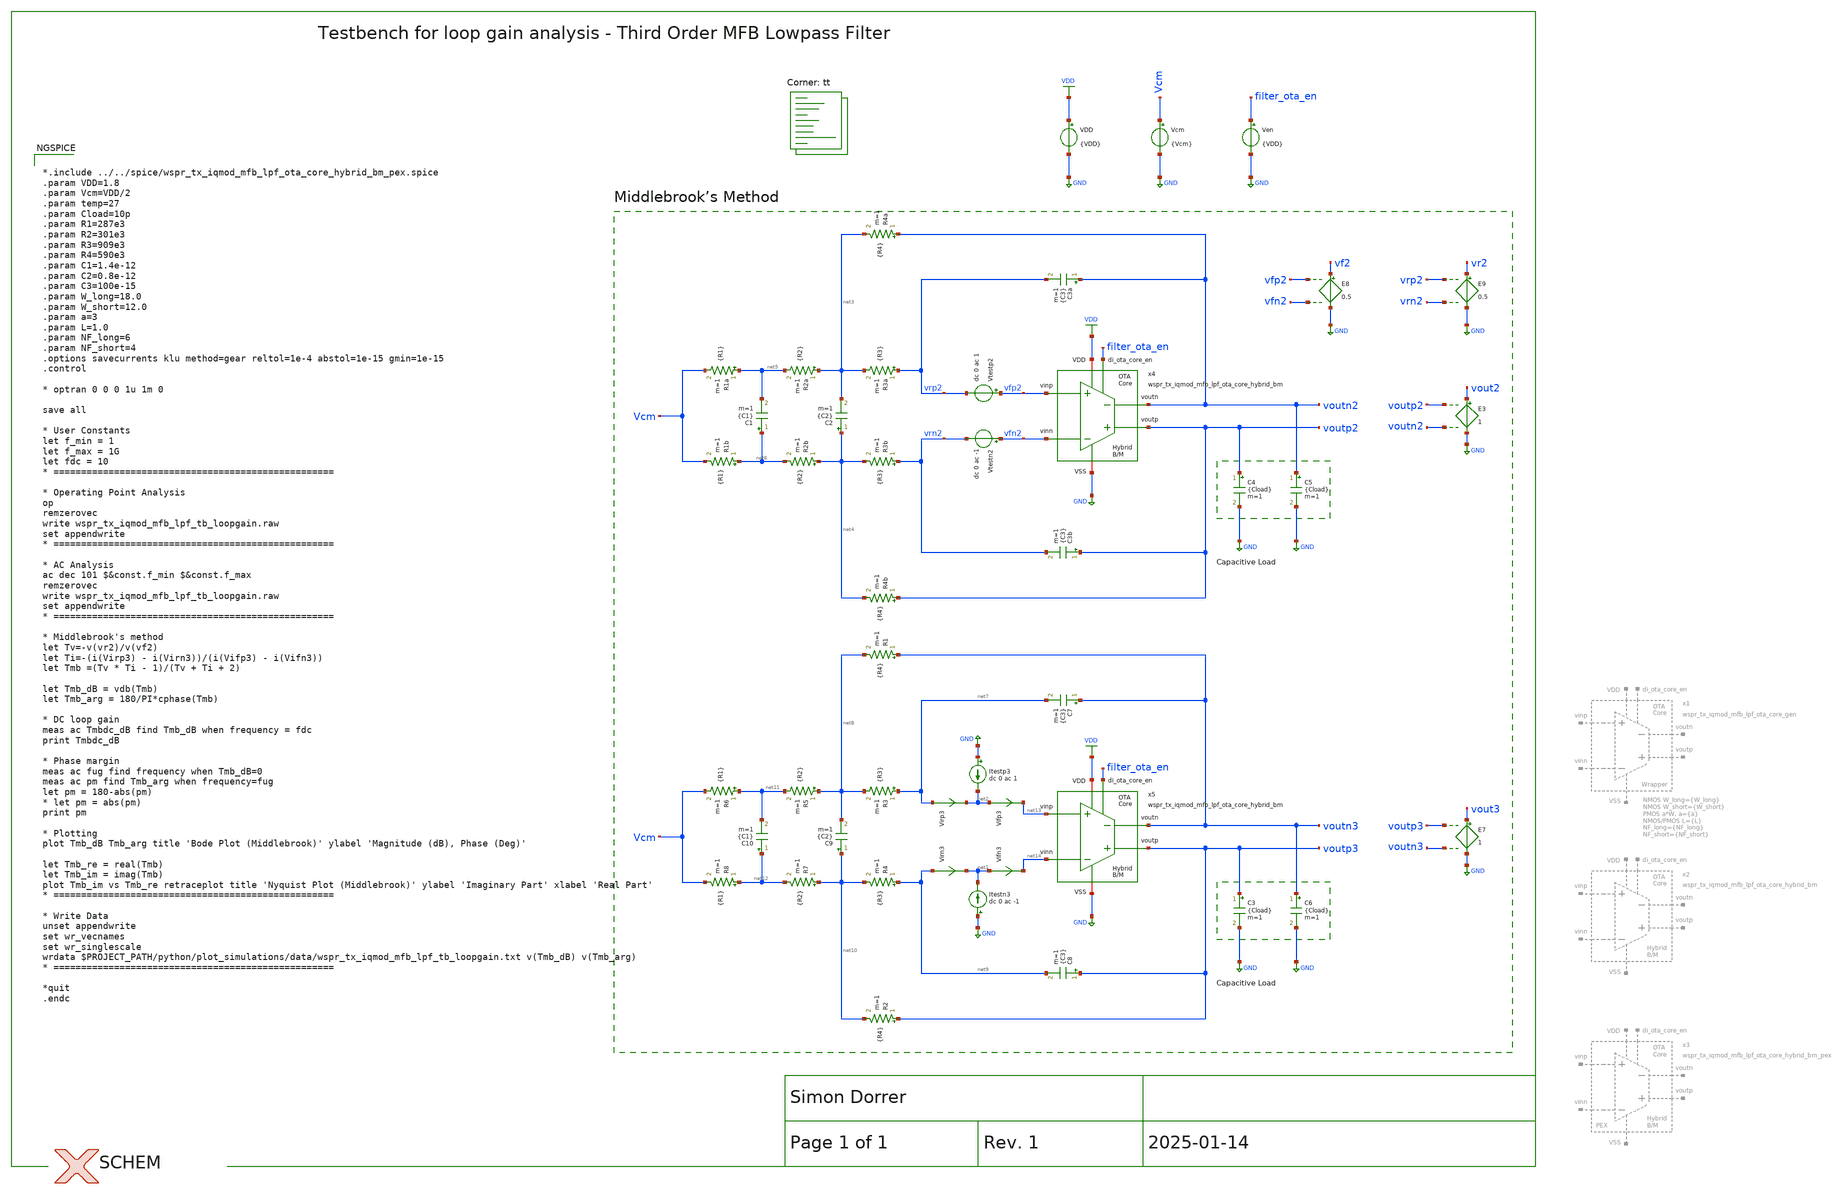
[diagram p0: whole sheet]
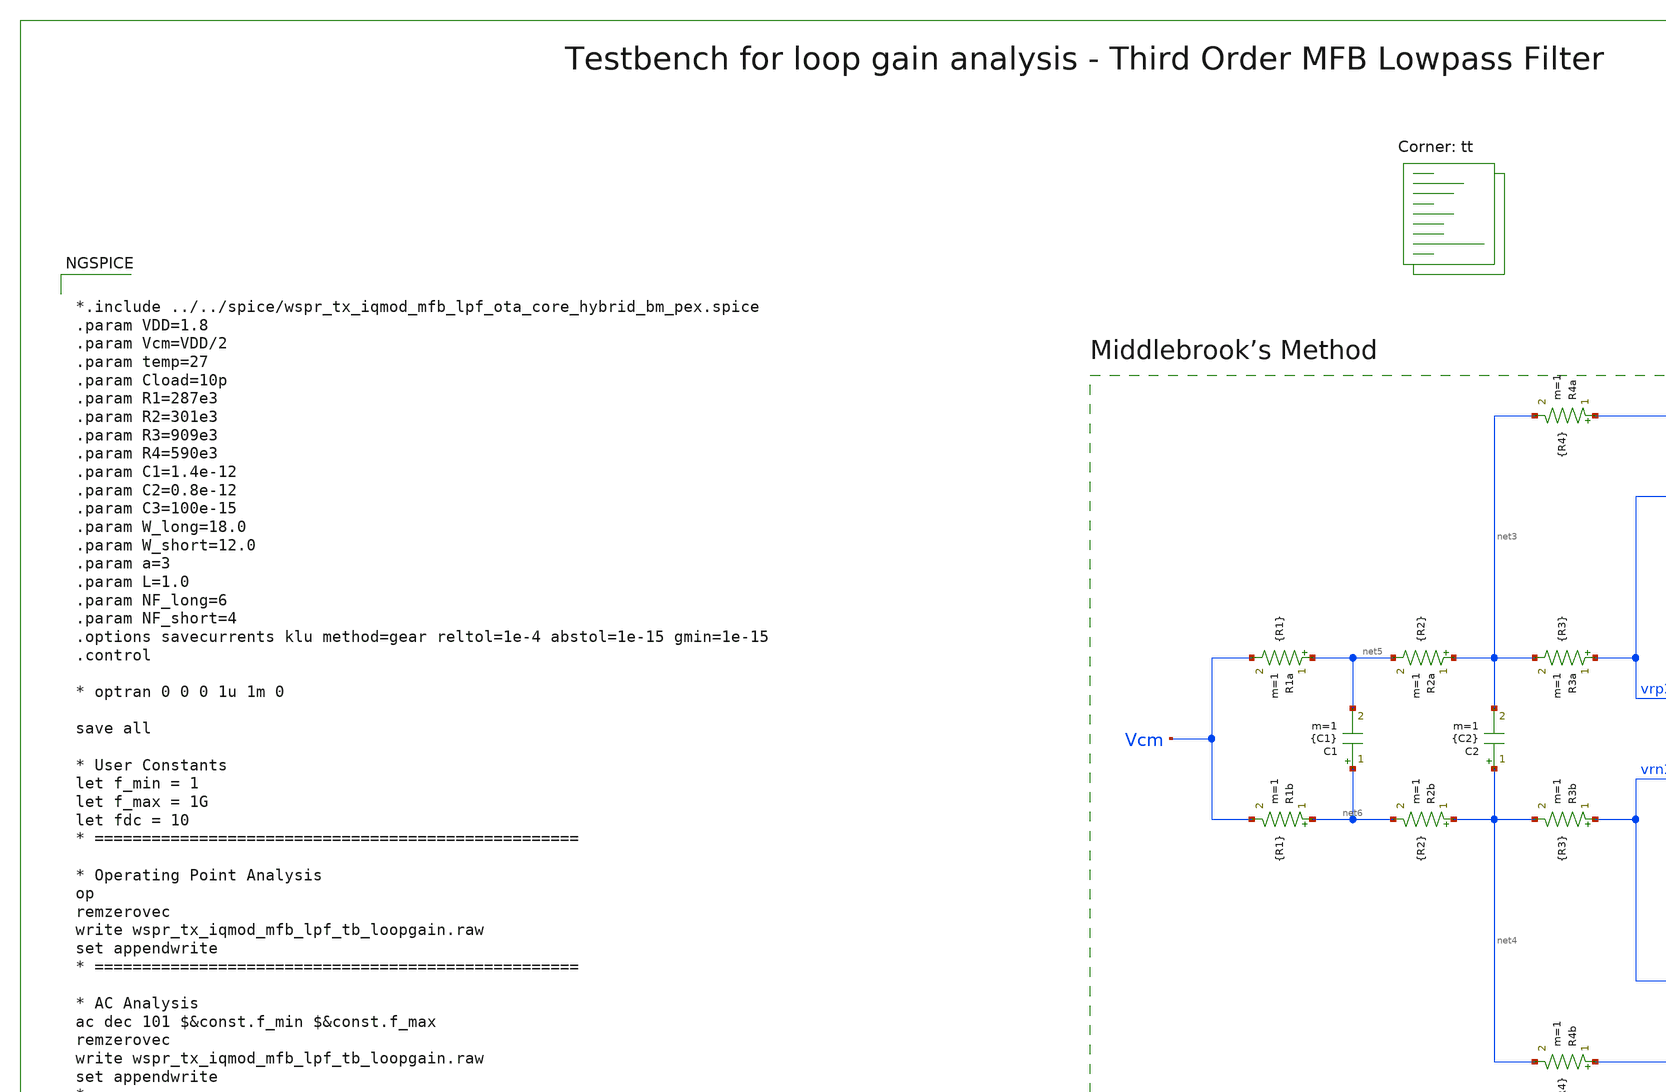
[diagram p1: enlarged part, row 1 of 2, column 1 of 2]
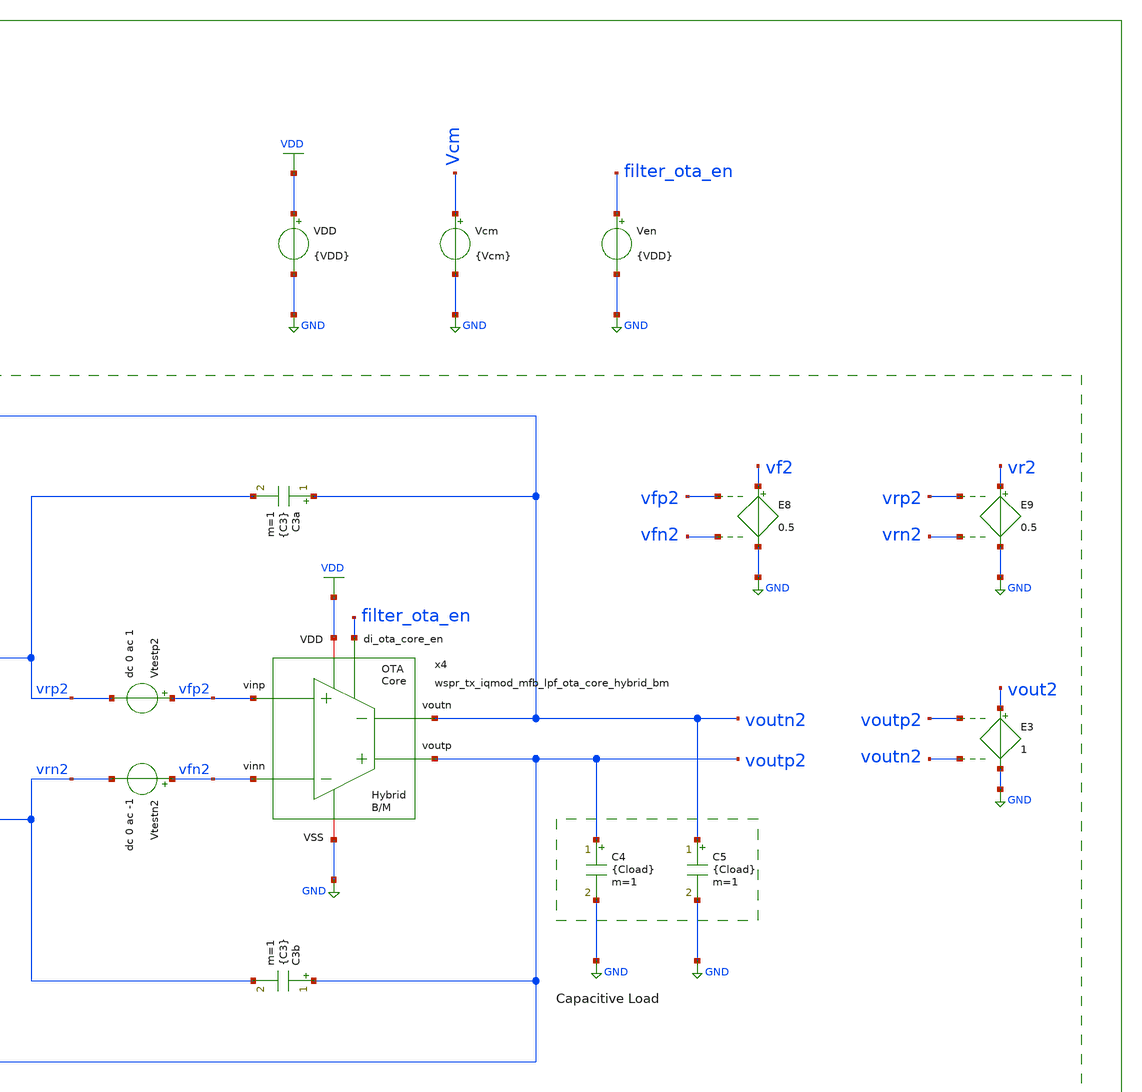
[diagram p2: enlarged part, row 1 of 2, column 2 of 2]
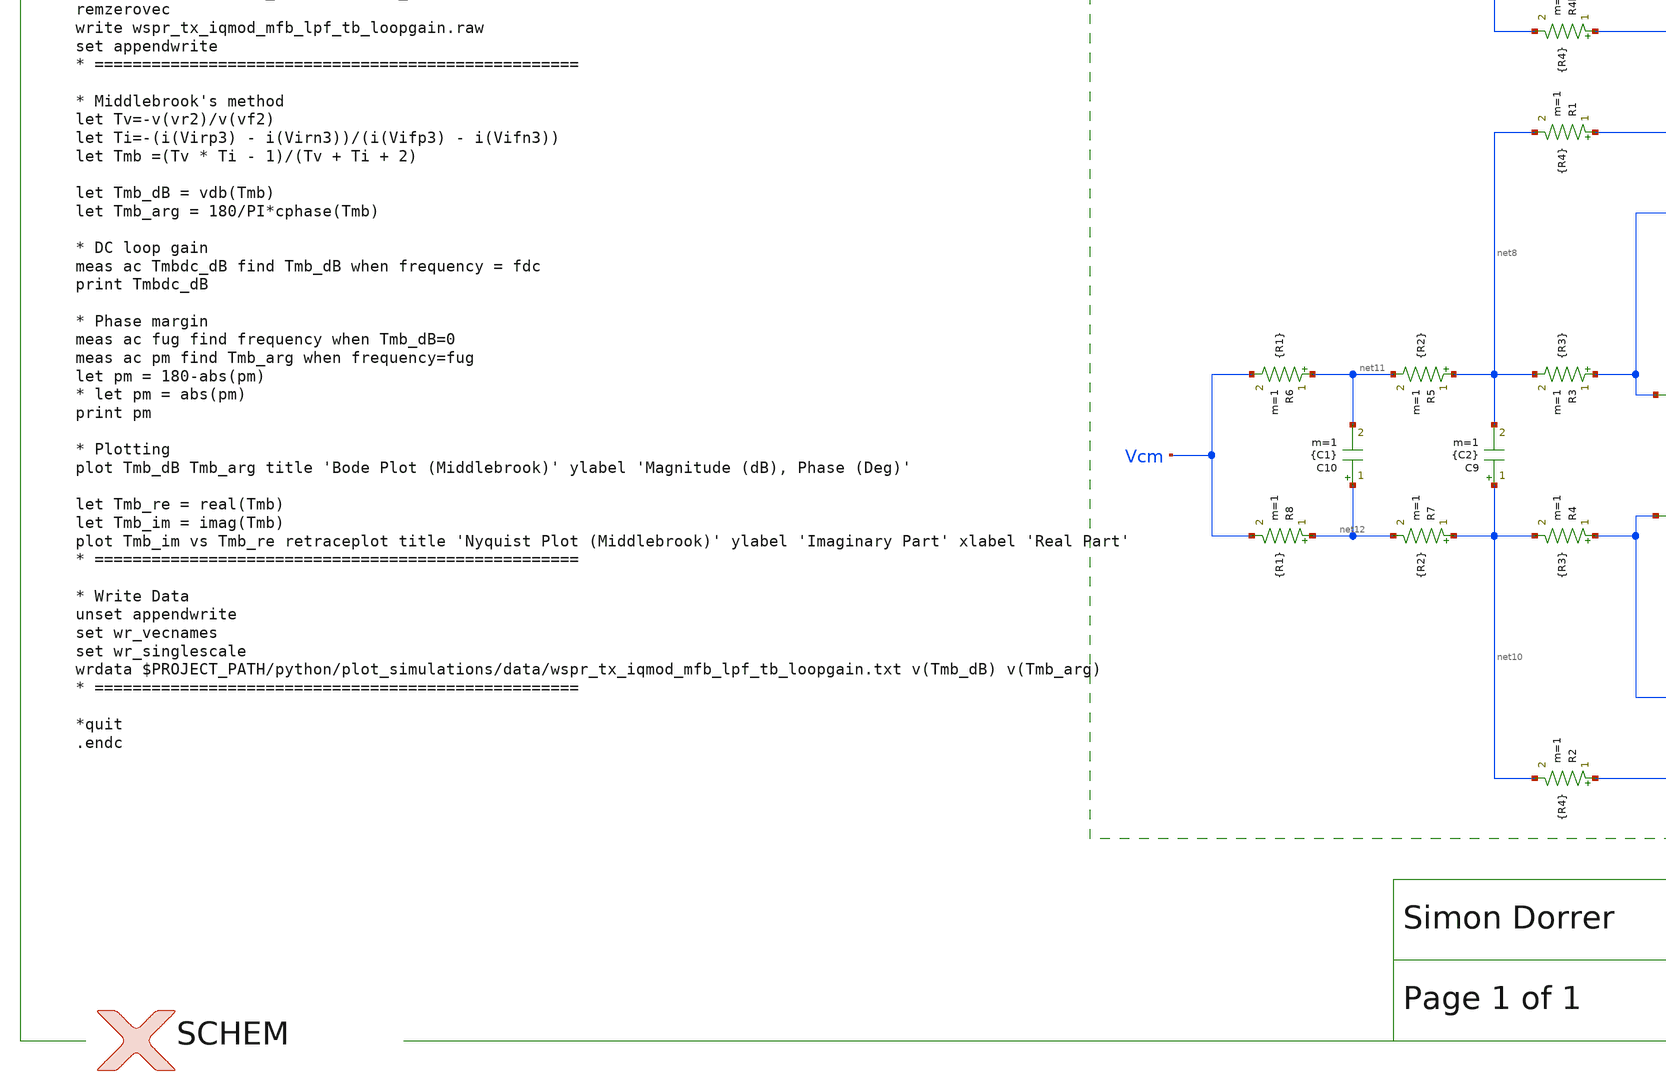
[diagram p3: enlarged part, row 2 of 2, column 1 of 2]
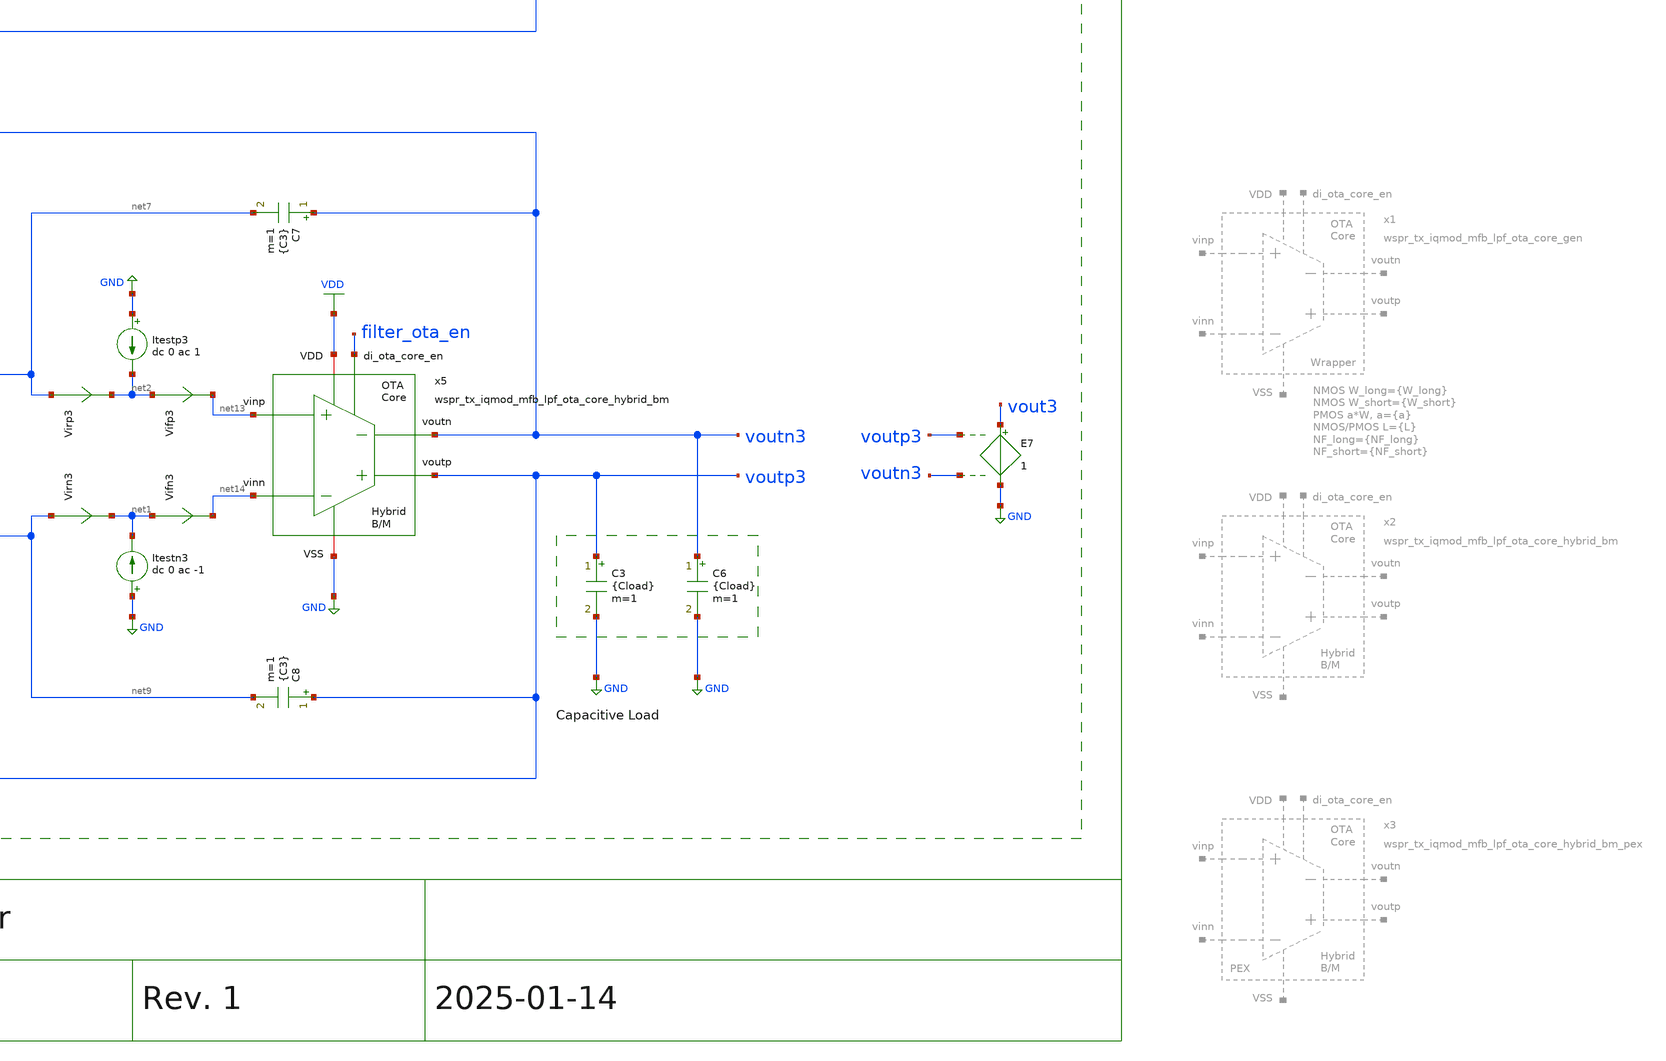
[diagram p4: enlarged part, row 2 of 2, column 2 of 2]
** sch_path: sky130/xschem/testbenches/wspr_tx_iqmod_mfb_lpf_tb_loopgain.sch
**.subckt wspr_tx_iqmod_mfb_lpf_tb_loopgain
VDD VDD GND {VDD}
Ven filter_ota_en GND {VDD}
C4 voutp2 GND {Cload} m=1
C5 voutn2 GND {Cload} m=1
E3 vout2 GND voutp2 voutn2 1
R4a voutn2 net3 {R4} m=1
R4b voutp2 net4 {R4} m=1
C3a voutn2 vrp2 {C3} m=1
C3b voutp2 vrn2 {C3} m=1
C2 net4 net3 {C2} m=1
E7 vout3 GND voutp3 voutn3 1
E8 vf2 GND vfp2 vfn2 0.5
E9 vr2 GND vrp2 vrn2 0.5
Vtestp2 vfp2 vrp2 dc 0 ac 1
Vtestn2 vfn2 vrn2 dc 0 ac -1
Virp3 net7 net2 0
.save i(virp3)
Vifp3 net2 net13 0
.save i(vifp3)
Itestn3 GND net1 dc 0 ac -1
Virn3 net9 net1 0
.save i(virn3)
Vifn3 net1 net14 0
.save i(vifn3)
Itestp3 GND net2 dc 0 ac 1
Vcm Vcm GND {Vcm}
R3a vrp2 net3 {R3} m=1
R3b vrn2 net4 {R3} m=1
R2a net3 net5 {R2} m=1
R1a net5 Vcm {R1} m=1
R2b net4 net6 {R2} m=1
R1b net6 Vcm {R1} m=1
C1 net6 net5 {C1} m=1
C3 voutp3 GND {Cload} m=1
C6 voutn3 GND {Cload} m=1
R1 voutn3 net8 {R4} m=1
R2 voutp3 net10 {R4} m=1
C7 voutn3 net7 {C3} m=1
C8 voutp3 net9 {C3} m=1
C9 net10 net8 {C2} m=1
R3 net7 net8 {R3} m=1
R4 net9 net10 {R3} m=1
R5 net8 net11 {R2} m=1
R6 net11 Vcm {R1} m=1
R7 net10 net12 {R2} m=1
R8 net12 Vcm {R1} m=1
C10 net12 net11 {C1} m=1
x4 filter_ota_en voutp2 voutn2 vfn2 vfp2 VDD GND wspr_tx_iqmod_mfb_lpf_ota_core_hybrid_bm
x5 filter_ota_en voutp3 voutn3 net14 net13 VDD GND wspr_tx_iqmod_mfb_lpf_ota_core_hybrid_bm
**** begin user architecture code


*.include ../../spice/wspr_tx_iqmod_mfb_lpf_ota_core_hybrid_bm_pex.spice
.param VDD=1.8
.param Vcm=VDD/2
.param temp=27
.param Cload=10p
.param R1=287e3
.param R2=301e3
.param R3=909e3
.param R4=590e3
.param C1=1.4e-12
.param C2=0.8e-12
.param C3=100e-15
.param W_long=18.0
.param W_short=12.0
.param a=3
.param L=1.0
.param NF_long=6
.param NF_short=4
.options savecurrents klu method=gear reltol=1e-4 abstol=1e-15 gmin=1e-15
.control

* optran 0 0 0 1u 1m 0

save all

* User Constants
let f_min = 1
let f_max = 1G
let fdc = 10
* ===================================================

* Operating Point Analysis
op
remzerovec
write wspr_tx_iqmod_mfb_lpf_tb_loopgain.raw
set appendwrite
* ===================================================

* AC Analysis
ac dec 101 $&const.f_min $&const.f_max
remzerovec
write wspr_tx_iqmod_mfb_lpf_tb_loopgain.raw
set appendwrite
* ===================================================

* Middlebrook's method
let Tv=-v(vr2)/v(vf2)
let Ti=-(i(Virp3) - i(Virn3))/(i(Vifp3) - i(Vifn3))
let Tmb =(Tv * Ti - 1)/(Tv + Ti + 2)

let Tmb_dB = vdb(Tmb)
let Tmb_arg = 180/PI*cphase(Tmb)

* DC loop gain
meas ac Tmbdc_dB find Tmb_dB when frequency = fdc
print Tmbdc_dB

* Phase margin
meas ac fug find frequency when Tmb_dB=0
meas ac pm find Tmb_arg when frequency=fug
let pm = 180-abs(pm)
* let pm = abs(pm)
print pm

* Plotting
plot Tmb_dB Tmb_arg title 'Bode Plot (Middlebrook)' ylabel 'Magnitude (dB), Phase (Deg)'

let Tmb_re = real(Tmb)
let Tmb_im = imag(Tmb)
plot Tmb_im vs Tmb_re retraceplot title 'Nyquist Plot (Middlebrook)' ylabel 'Imaginary Part' xlabel 'Real
+ Part'
* ===================================================

* Write Data
unset appendwrite
set wr_vecnames
set wr_singlescale
wrdata $PROJECT_PATH/python/plot_simulations/data/wspr_tx_iqmod_mfb_lpf_tb_loopgain.txt v(Tmb_dB) v(Tmb_arg)
* ===================================================

*quit
.endc


.lib $::SKYWATER_MODELS/sky130.lib.spice tt
**** end user architecture code
**.ends
.GLOBAL GND
.GLOBAL VDD
.end
